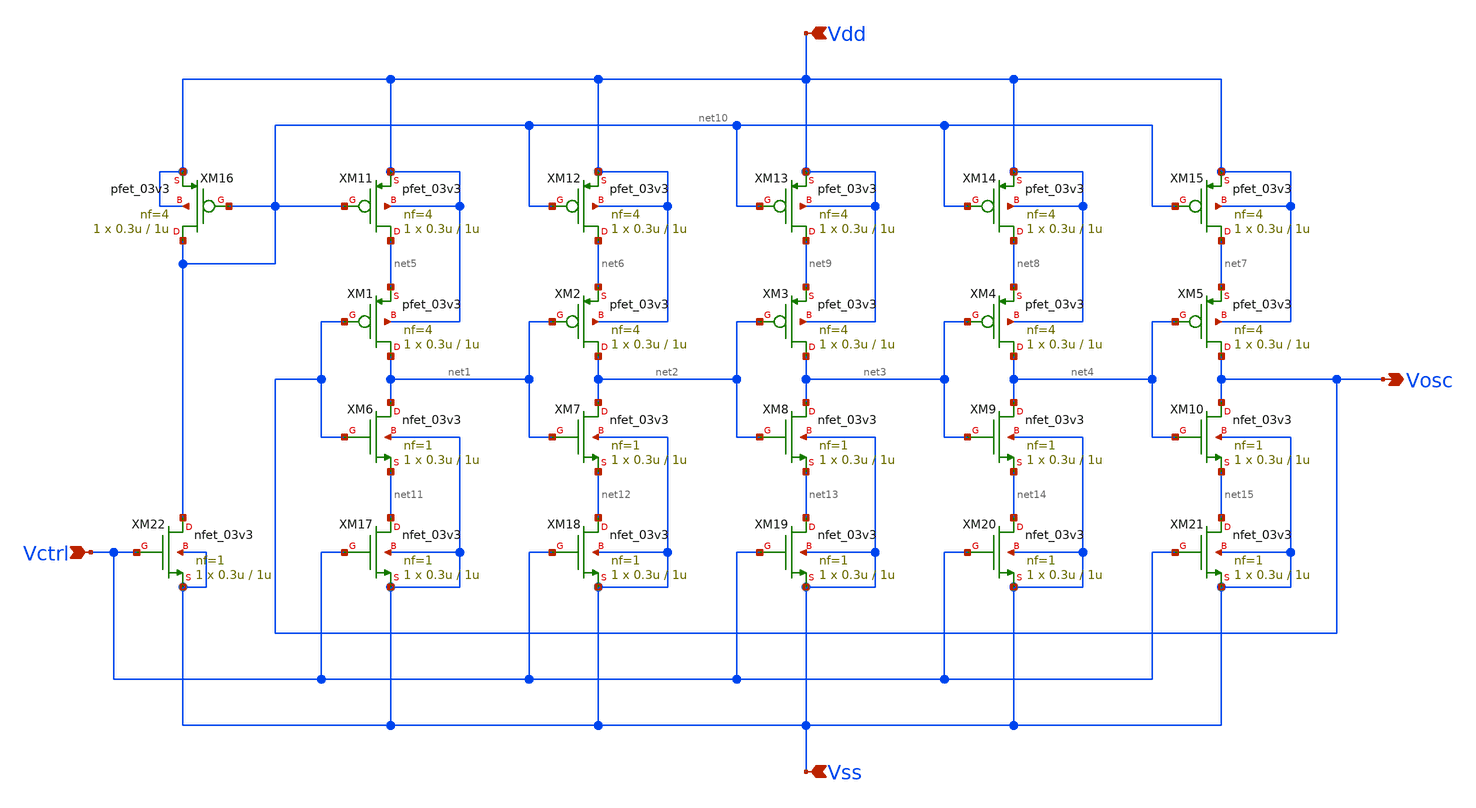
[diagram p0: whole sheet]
** sch_path: Project/1-on-chip/schematic/VCO/ring-vco/five-stage-ring.sch
**.subckt five-stage-ring Vdd Vctrl Vss Vosc
*.ipin Vdd
*.ipin Vctrl
*.ipin Vss
*.opin Vosc
XM1 net1 Vosc net5 Vdd pfet_03v3 L=1u W=0.3u nf=4 ad='int((nf+1)/2) * W/nf * 0.18u' as='int((nf+2)/2) * W/nf * 0.18u'
+ pd='2*int((nf+1)/2) * (W/nf + 0.18u)' ps='2*int((nf+2)/2) * (W/nf + 0.18u)' nrd='0.18u / W' nrs='0.18u / W'
+ sa=0 sb=0 sd=0 m=1
XM2 net2 net1 net6 Vdd pfet_03v3 L=1u W=0.3u nf=4 ad='int((nf+1)/2) * W/nf * 0.18u' as='int((nf+2)/2) * W/nf * 0.18u'
+ pd='2*int((nf+1)/2) * (W/nf + 0.18u)' ps='2*int((nf+2)/2) * (W/nf + 0.18u)' nrd='0.18u / W' nrs='0.18u / W'
+ sa=0 sb=0 sd=0 m=1
XM3 net3 net2 net9 Vdd pfet_03v3 L=1u W=0.3u nf=4 ad='int((nf+1)/2) * W/nf * 0.18u' as='int((nf+2)/2) * W/nf * 0.18u'
+ pd='2*int((nf+1)/2) * (W/nf + 0.18u)' ps='2*int((nf+2)/2) * (W/nf + 0.18u)' nrd='0.18u / W' nrs='0.18u / W'
+ sa=0 sb=0 sd=0 m=1
XM4 net4 net3 net8 Vdd pfet_03v3 L=1u W=0.3u nf=4 ad='int((nf+1)/2) * W/nf * 0.18u' as='int((nf+2)/2) * W/nf * 0.18u'
+ pd='2*int((nf+1)/2) * (W/nf + 0.18u)' ps='2*int((nf+2)/2) * (W/nf + 0.18u)' nrd='0.18u / W' nrs='0.18u / W'
+ sa=0 sb=0 sd=0 m=1
XM5 Vosc net4 net7 Vdd pfet_03v3 L=1u W=0.3u nf=4 ad='int((nf+1)/2) * W/nf * 0.18u' as='int((nf+2)/2) * W/nf * 0.18u'
+ pd='2*int((nf+1)/2) * (W/nf + 0.18u)' ps='2*int((nf+2)/2) * (W/nf + 0.18u)' nrd='0.18u / W' nrs='0.18u / W'
+ sa=0 sb=0 sd=0 m=1
XM6 net1 Vosc net11 Vss nfet_03v3 L=1u W=0.3u nf=1 ad='int((nf+1)/2) * W/nf * 0.18u' as='int((nf+2)/2) * W/nf * 0.18u'
+ pd='2*int((nf+1)/2) * (W/nf + 0.18u)' ps='2*int((nf+2)/2) * (W/nf + 0.18u)' nrd='0.18u / W' nrs='0.18u / W'
+ sa=0 sb=0 sd=0 m=1
XM7 net2 net1 net12 Vss nfet_03v3 L=1u W=0.3u nf=1 ad='int((nf+1)/2) * W/nf * 0.18u' as='int((nf+2)/2) * W/nf * 0.18u'
+ pd='2*int((nf+1)/2) * (W/nf + 0.18u)' ps='2*int((nf+2)/2) * (W/nf + 0.18u)' nrd='0.18u / W' nrs='0.18u / W'
+ sa=0 sb=0 sd=0 m=1
XM8 net3 net2 net13 Vss nfet_03v3 L=1u W=0.3u nf=1 ad='int((nf+1)/2) * W/nf * 0.18u' as='int((nf+2)/2) * W/nf * 0.18u'
+ pd='2*int((nf+1)/2) * (W/nf + 0.18u)' ps='2*int((nf+2)/2) * (W/nf + 0.18u)' nrd='0.18u / W' nrs='0.18u / W'
+ sa=0 sb=0 sd=0 m=1
XM9 net4 net3 net14 Vss nfet_03v3 L=1u W=0.3u nf=1 ad='int((nf+1)/2) * W/nf * 0.18u' as='int((nf+2)/2) * W/nf * 0.18u'
+ pd='2*int((nf+1)/2) * (W/nf + 0.18u)' ps='2*int((nf+2)/2) * (W/nf + 0.18u)' nrd='0.18u / W' nrs='0.18u / W'
+ sa=0 sb=0 sd=0 m=1
XM10 Vosc net4 net15 Vss nfet_03v3 L=1u W=0.3u nf=1 ad='int((nf+1)/2) * W/nf * 0.18u' as='int((nf+2)/2) * W/nf * 0.18u'
+ pd='2*int((nf+1)/2) * (W/nf + 0.18u)' ps='2*int((nf+2)/2) * (W/nf + 0.18u)' nrd='0.18u / W' nrs='0.18u / W'
+ sa=0 sb=0 sd=0 m=1
XM11 net5 net10 Vdd Vdd pfet_03v3 L=1u W=0.3u nf=4 ad='int((nf+1)/2) * W/nf * 0.18u' as='int((nf+2)/2) * W/nf * 0.18u'
+ pd='2*int((nf+1)/2) * (W/nf + 0.18u)' ps='2*int((nf+2)/2) * (W/nf + 0.18u)' nrd='0.18u / W' nrs='0.18u / W'
+ sa=0 sb=0 sd=0 m=1
XM12 net6 net10 Vdd Vdd pfet_03v3 L=1u W=0.3u nf=4 ad='int((nf+1)/2) * W/nf * 0.18u' as='int((nf+2)/2) * W/nf * 0.18u'
+ pd='2*int((nf+1)/2) * (W/nf + 0.18u)' ps='2*int((nf+2)/2) * (W/nf + 0.18u)' nrd='0.18u / W' nrs='0.18u / W'
+ sa=0 sb=0 sd=0 m=1
XM13 net9 net10 Vdd Vdd pfet_03v3 L=1u W=0.3u nf=4 ad='int((nf+1)/2) * W/nf * 0.18u' as='int((nf+2)/2) * W/nf * 0.18u'
+ pd='2*int((nf+1)/2) * (W/nf + 0.18u)' ps='2*int((nf+2)/2) * (W/nf + 0.18u)' nrd='0.18u / W' nrs='0.18u / W'
+ sa=0 sb=0 sd=0 m=1
XM14 net8 net10 Vdd Vdd pfet_03v3 L=1u W=0.3u nf=4 ad='int((nf+1)/2) * W/nf * 0.18u' as='int((nf+2)/2) * W/nf * 0.18u'
+ pd='2*int((nf+1)/2) * (W/nf + 0.18u)' ps='2*int((nf+2)/2) * (W/nf + 0.18u)' nrd='0.18u / W' nrs='0.18u / W'
+ sa=0 sb=0 sd=0 m=1
XM15 net7 net10 Vdd Vdd pfet_03v3 L=1u W=0.3u nf=4 ad='int((nf+1)/2) * W/nf * 0.18u' as='int((nf+2)/2) * W/nf * 0.18u'
+ pd='2*int((nf+1)/2) * (W/nf + 0.18u)' ps='2*int((nf+2)/2) * (W/nf + 0.18u)' nrd='0.18u / W' nrs='0.18u / W'
+ sa=0 sb=0 sd=0 m=1
XM16 net10 net10 Vdd Vdd pfet_03v3 L=1u W=0.3u nf=4 ad='int((nf+1)/2) * W/nf * 0.18u' as='int((nf+2)/2) * W/nf * 0.18u'
+ pd='2*int((nf+1)/2) * (W/nf + 0.18u)' ps='2*int((nf+2)/2) * (W/nf + 0.18u)' nrd='0.18u / W' nrs='0.18u / W'
+ sa=0 sb=0 sd=0 m=1
XM17 net11 Vctrl Vss Vss nfet_03v3 L=1u W=0.3u nf=1 ad='int((nf+1)/2) * W/nf * 0.18u' as='int((nf+2)/2) * W/nf * 0.18u'
+ pd='2*int((nf+1)/2) * (W/nf + 0.18u)' ps='2*int((nf+2)/2) * (W/nf + 0.18u)' nrd='0.18u / W' nrs='0.18u / W'
+ sa=0 sb=0 sd=0 m=1
XM18 net12 Vctrl Vss Vss nfet_03v3 L=1u W=0.3u nf=1 ad='int((nf+1)/2) * W/nf * 0.18u' as='int((nf+2)/2) * W/nf * 0.18u'
+ pd='2*int((nf+1)/2) * (W/nf + 0.18u)' ps='2*int((nf+2)/2) * (W/nf + 0.18u)' nrd='0.18u / W' nrs='0.18u / W'
+ sa=0 sb=0 sd=0 m=1
XM19 net13 Vctrl Vss Vss nfet_03v3 L=1u W=0.3u nf=1 ad='int((nf+1)/2) * W/nf * 0.18u' as='int((nf+2)/2) * W/nf * 0.18u'
+ pd='2*int((nf+1)/2) * (W/nf + 0.18u)' ps='2*int((nf+2)/2) * (W/nf + 0.18u)' nrd='0.18u / W' nrs='0.18u / W'
+ sa=0 sb=0 sd=0 m=1
XM20 net14 Vctrl Vss Vss nfet_03v3 L=1u W=0.3u nf=1 ad='int((nf+1)/2) * W/nf * 0.18u' as='int((nf+2)/2) * W/nf * 0.18u'
+ pd='2*int((nf+1)/2) * (W/nf + 0.18u)' ps='2*int((nf+2)/2) * (W/nf + 0.18u)' nrd='0.18u / W' nrs='0.18u / W'
+ sa=0 sb=0 sd=0 m=1
XM21 net15 Vctrl Vss Vss nfet_03v3 L=1u W=0.3u nf=1 ad='int((nf+1)/2) * W/nf * 0.18u' as='int((nf+2)/2) * W/nf * 0.18u'
+ pd='2*int((nf+1)/2) * (W/nf + 0.18u)' ps='2*int((nf+2)/2) * (W/nf + 0.18u)' nrd='0.18u / W' nrs='0.18u / W'
+ sa=0 sb=0 sd=0 m=1
XM22 net10 Vctrl Vss Vss nfet_03v3 L=1u W=0.3u nf=1 ad='int((nf+1)/2) * W/nf * 0.18u' as='int((nf+2)/2) * W/nf * 0.18u'
+ pd='2*int((nf+1)/2) * (W/nf + 0.18u)' ps='2*int((nf+2)/2) * (W/nf + 0.18u)' nrd='0.18u / W' nrs='0.18u / W'
+ sa=0 sb=0 sd=0 m=1
**.ends
.end
